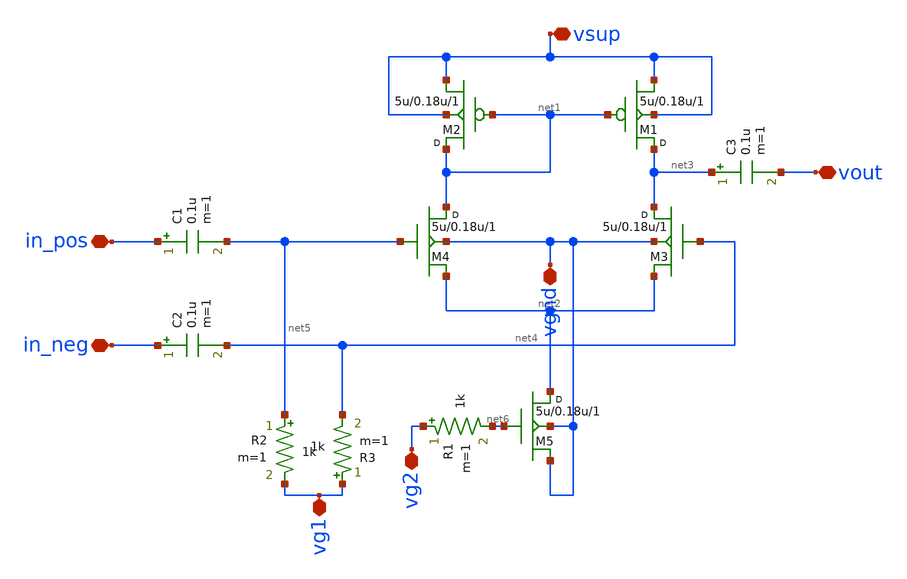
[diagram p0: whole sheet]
** sch_path: dev/balun/balun.sch
**.subckt balun vgnd vsup in_neg in_pos vout vg1 vg2
*.iopin vgnd
*.iopin vsup
*.iopin in_neg
*.iopin in_pos
*.iopin vout
*.iopin vg1
*.iopin vg2
M1 net3 net1 vsup vsup pmos w=5u l=0.18u m=1
M2 net1 net1 vsup vsup pmos w=5u l=0.18u m=1
M3 net3 net4 net2 vgnd nmos w=5u l=0.18u m=1
M4 net1 net5 net2 vgnd nmos w=5u l=0.18u m=1
M5 net2 net6 vgnd vgnd nmos w=5u l=0.18u m=1
C1 in_pos net5 0.1u m=1
C2 in_neg net4 0.1u m=1
C3 net3 vout 0.1u m=1
R1 vg2 net6 1k m=1
R2 net5 vg1 1k m=1
R3 vg1 net4 1k m=1
**.ends
.end
